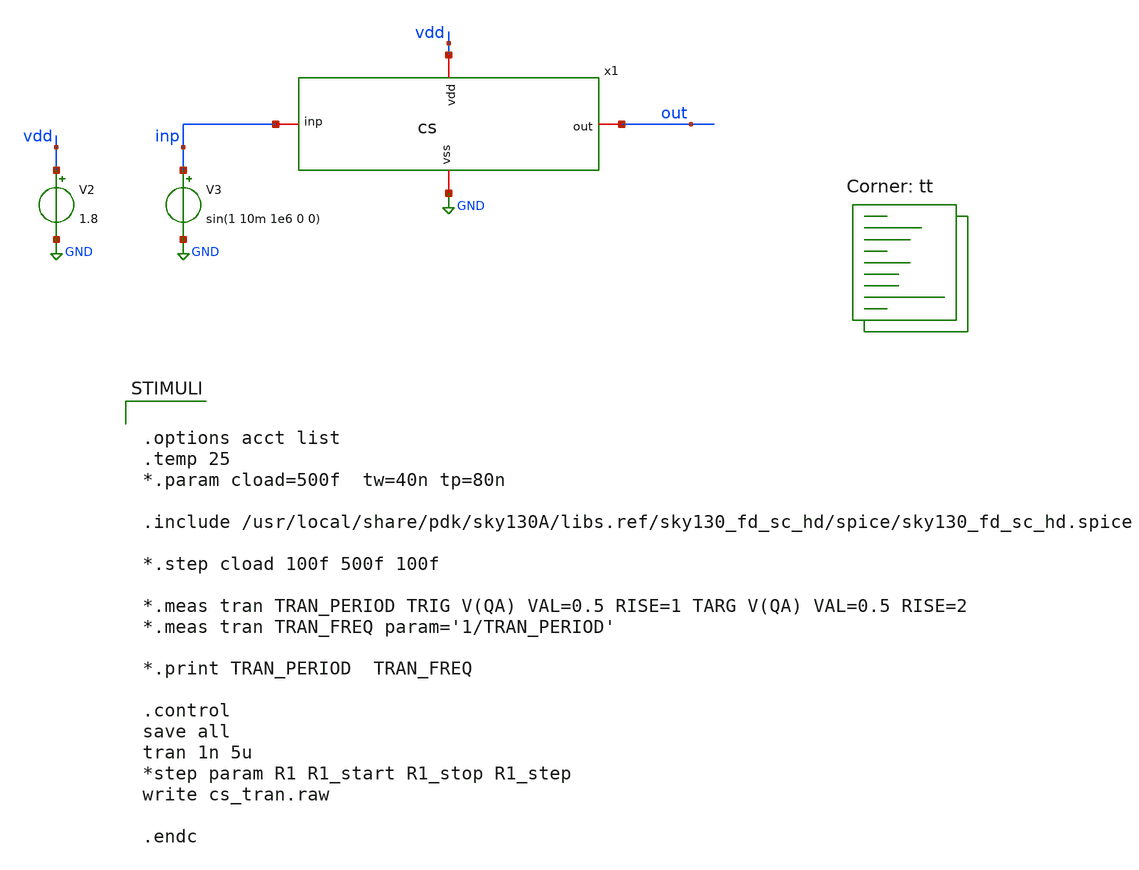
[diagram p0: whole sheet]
** sch_path: xschem/untitled-4.sch
**.subckt untitled-4
x1 vdd out inp GND cs
V2 vdd GND 1.8
V3 inp GND sin(1 10m 1e6 0 0)
**** begin user architecture code
.lib $::SKYWATER_MODELS/sky130.lib.spice tt


.options acct list
.temp 25
*.param cload=500f  tw=40n tp=80n

.include /usr/local/share/pdk/sky130A/libs.ref/sky130_fd_sc_hd/spice/sky130_fd_sc_hd.spice

*.step cload 100f 500f 100f

*.meas tran TRAN_PERIOD TRIG V(QA) VAL=0.5 RISE=1 TARG V(QA) VAL=0.5 RISE=2
*.meas tran TRAN_FREQ param='1/TRAN_PERIOD'

*.print TRAN_PERIOD  TRAN_FREQ

.control
save all
tran 1n 5u
*step param R1 R1_start R1_stop R1_step
write cs_tran.raw

.endc


**** end user architecture code
**.ends

* expanding   symbol:  cs/cs.sym # of pins=4
** sym_path: xschem/cs/cs.sym
** sch_path: xschem/cs/cs.sch
.subckt cs vdd out inp vss
*.iopin inp
*.iopin out
*.iopin vdd
*.iopin vss
XM1 out inp vss vss sky130_fd_pr__nfet_01v8 L=0.15 W=50 nf=1 ad='int((nf+1)/2) * W/nf * 0.29' as='int((nf+2)/2) * W/nf * 0.29'
+ pd='2*int((nf+1)/2) * (W/nf + 0.29)' ps='2*int((nf+2)/2) * (W/nf + 0.29)' nrd='0.29 / W' nrs='0.29 / W'
+ sa=0 sb=0 sd=0 mult=1 m=1
XR1 out vdd vss sky130_fd_pr__res_high_po_1p41 L=0.5 mult=1 m=1
.ends

.GLOBAL GND
.end
